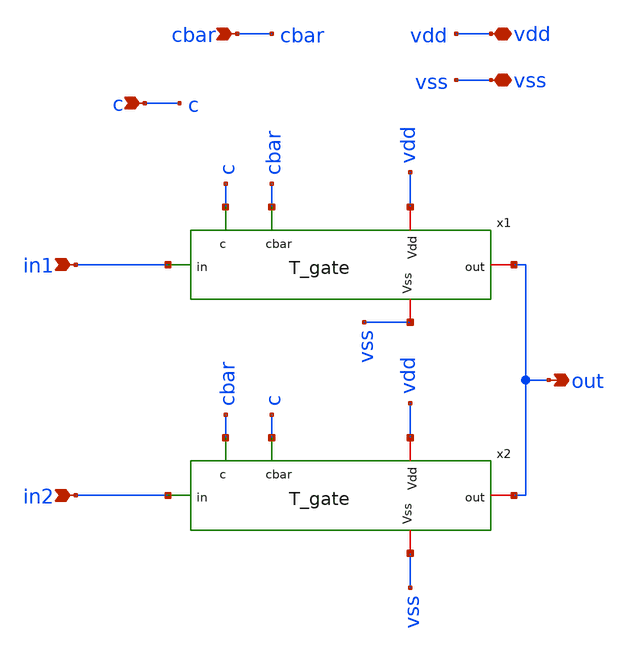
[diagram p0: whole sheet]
** sch_path: ADC/4bit_C2C/MagicAndSpice/SPDT.sch
**.subckt SPDT in1 in2 c cbar out vdd vss
*.ipin in1
*.ipin in2
*.ipin c
*.ipin cbar
*.opin out
*.iopin vdd
*.iopin vss
x1 c out in1 vdd cbar vss T_gate
x2 cbar out in2 vdd c vss T_gate
**** begin user architecture code

** opencircuitdesign pdks install
.lib $::SKYWATER_MODELS/sky130.lib.spice tt


**** end user architecture code
**.ends
.end
